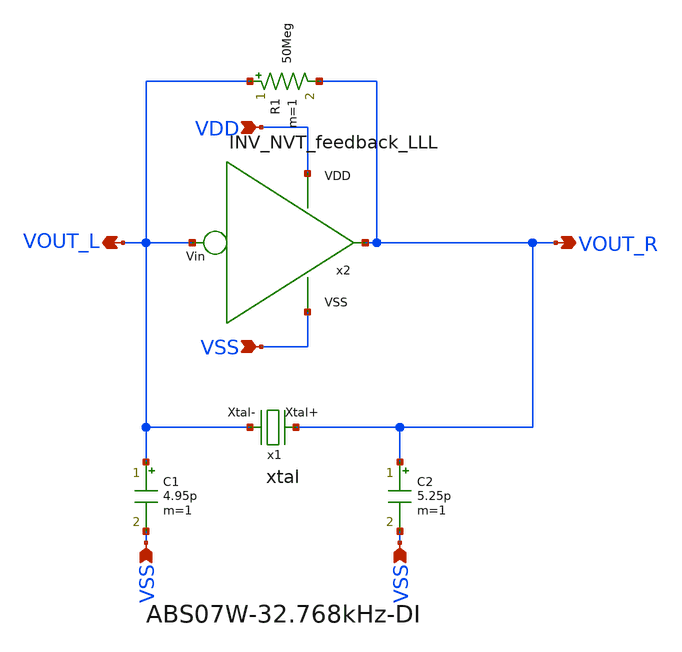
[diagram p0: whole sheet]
** sch_path: design/THESIS_EXP_RO_INVERTER_SKY130A/xtal_osc_NVT_LLL.sch
**.subckt xtal_osc_NVT_LLL VSS VSS VOUT_R VOUT_L VDD VSS
*.ipin VSS
*.ipin VSS
*.opin VOUT_R
*.opin VOUT_L
*.ipin VDD
*.ipin VSS
x1 VOUT_R VOUT_L xtal
C1 VOUT_L VSS 4.95p m=1
C2 VOUT_R VSS 5.25p m=1
R1 VOUT_L VOUT_R 50Meg m=1
x2 VOUT_R VDD VSS VOUT_L INV_NVT_feedback_LLL
**.ends

* expanding   symbol:  THESIS_EXP_RO_INVERTER_SKY130A/xtal.sym # of pins=2
** sym_path: design/THESIS_EXP_RO_INVERTER_SKY130A/xtal.sym
** sch_path: design/THESIS_EXP_RO_INVERTER_SKY130A/xtal.sch
.subckt xtal Xtal+ Xtal-
*.iopin Xtal+
*.iopin Xtal-
R1 Xtal+ net1 38.194k m=1
C1 net1 net2 4.68f m=1
L1 net2 Xtal- 5048.571 m=1
C2 Xtal+ Xtal- 1.15p m=1
.ends


* expanding   symbol:  THESIS_EXP_RO_INVERTER_SKY130A/INV_NVT_feedback_LLL.sym # of pins=4
** sym_path: design/THESIS_EXP_RO_INVERTER_SKY130A/INV_NVT_feedback_LLL.sym
** sch_path: design/THESIS_EXP_RO_INVERTER_SKY130A/INV_NVT_feedback_LLL.sch
.subckt INV_NVT_feedback_LLL Vout VDD VSS Vin
*.ipin VSS
*.ipin Vin
*.opin Vout
*.ipin VDD
XM1 net2 Vin VDD VDD sky130_fd_pr__pfet_01v8_lvt L=0.35 W=7 nf=1 ad='int((nf+1)/2) * W/nf * 0.29' as='int((nf+2)/2) * W/nf * 0.29'
+ pd='2*int((nf+1)/2) * (W/nf + 0.29)' ps='2*int((nf+2)/2) * (W/nf + 0.29)' nrd='0.29 / W' nrs='0.29 / W'
+ sa=0 sb=0 sd=0 mult=m_alpha m=m_alpha
XM2 net3 Vin vn VSS sky130_fd_pr__nfet_03v3_nvt L=0.6 W=1 nf=1 ad='int((nf+1)/2) * W/nf * 0.29' as='int((nf+2)/2) * W/nf * 0.29'
+ pd='2*int((nf+1)/2) * (W/nf + 0.29)' ps='2*int((nf+2)/2) * (W/nf + 0.29)' nrd='0.29 / W' nrs='0.29 / W'
+ sa=0 sb=0 sd=0 mult=m_beta m=m_beta
XM3 net1 Vin VSS VSS sky130_fd_pr__nfet_03v3_nvt L=0.6 W=1 nf=1 ad='int((nf+1)/2) * W/nf * 0.29' as='int((nf+2)/2) * W/nf * 0.29'
+ pd='2*int((nf+1)/2) * (W/nf + 0.29)' ps='2*int((nf+2)/2) * (W/nf + 0.29)' nrd='0.29 / W' nrs='0.29 / W'
+ sa=0 sb=0 sd=0 mult=m_I0 m=m_I0
XM4 VDD Vout net4 VSS sky130_fd_pr__nfet_03v3_nvt L=0.6 W=1 nf=1 ad='int((nf+1)/2) * W/nf * 0.29' as='int((nf+2)/2) * W/nf * 0.29'
+ pd='2*int((nf+1)/2) * (W/nf + 0.29)' ps='2*int((nf+2)/2) * (W/nf + 0.29)' nrd='0.29 / W' nrs='0.29 / W'
+ sa=0 sb=0 sd=0 mult=m_gamma m=m_gamma
XM5 Vout Vin net3 VSS sky130_fd_pr__nfet_03v3_nvt L=0.6 W=1 nf=1 ad='int((nf+1)/2) * W/nf * 0.29' as='int((nf+2)/2) * W/nf * 0.29'
+ pd='2*int((nf+1)/2) * (W/nf + 0.29)' ps='2*int((nf+2)/2) * (W/nf + 0.29)' nrd='0.29 / W' nrs='0.29 / W'
+ sa=0 sb=0 sd=0 mult=m_beta m=m_beta
XM6 vn Vin net1 VSS sky130_fd_pr__nfet_03v3_nvt L=0.6 W=1 nf=1 ad='int((nf+1)/2) * W/nf * 0.29' as='int((nf+2)/2) * W/nf * 0.29'
+ pd='2*int((nf+1)/2) * (W/nf + 0.29)' ps='2*int((nf+2)/2) * (W/nf + 0.29)' nrd='0.29 / W' nrs='0.29 / W'
+ sa=0 sb=0 sd=0 mult=m_I0 m=m_I0
XM7 net4 Vout vn VSS sky130_fd_pr__nfet_03v3_nvt L=0.6 W=1 nf=1 ad='int((nf+1)/2) * W/nf * 0.29' as='int((nf+2)/2) * W/nf * 0.29'
+ pd='2*int((nf+1)/2) * (W/nf + 0.29)' ps='2*int((nf+2)/2) * (W/nf + 0.29)' nrd='0.29 / W' nrs='0.29 / W'
+ sa=0 sb=0 sd=0 mult=m_gamma m=m_gamma
XM8 Vout Vin net2 VDD sky130_fd_pr__pfet_01v8_lvt L=0.35 W=7 nf=1 ad='int((nf+1)/2) * W/nf * 0.29' as='int((nf+2)/2) * W/nf * 0.29'
+ pd='2*int((nf+1)/2) * (W/nf + 0.29)' ps='2*int((nf+2)/2) * (W/nf + 0.29)' nrd='0.29 / W' nrs='0.29 / W'
+ sa=0 sb=0 sd=0 mult=m_alpha m=m_alpha
.ends

.end
